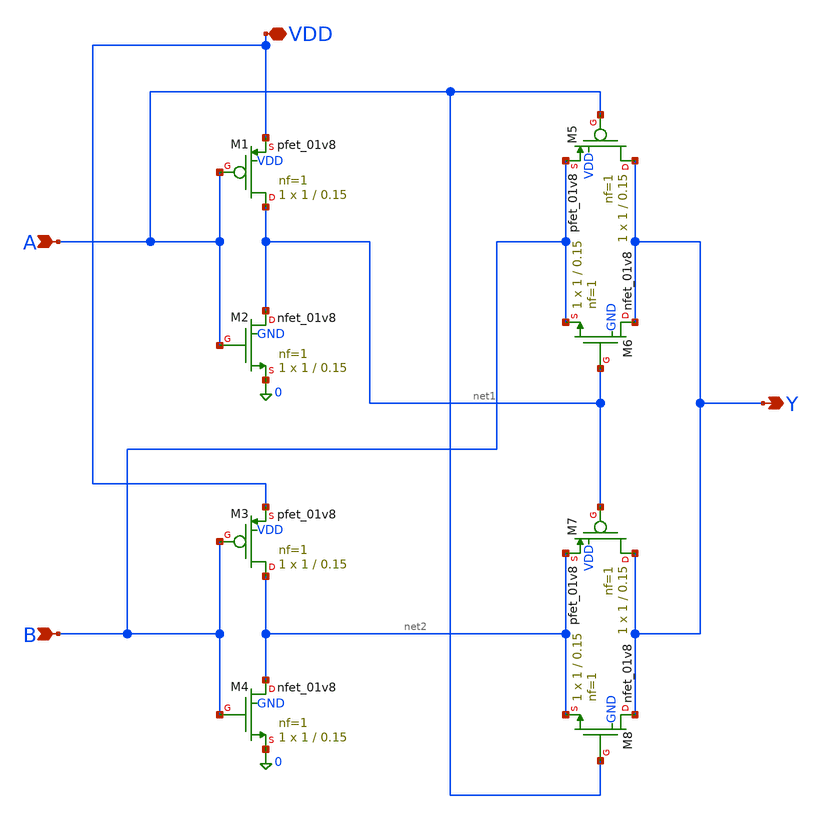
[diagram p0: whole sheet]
** sch_path: schematic/xor.sch
**.subckt xor VDD A B Y
*.iopin VDD
*.ipin A
*.ipin B
*.opin Y
XM1 net1 A VDD VDD sky130_fd_pr__pfet_01v8 L=0.15 W=1 nf=1 ad='int((1 + 1)/2) * 1 / 1 * 0.29' as='int((1 + 2)/2) * 1 / 1 * 0.29'
+ pd='2*int((1 + 1)/2) * (1 / 1 + 0.29)' ps='2*int((1 + 2)/2) * (1 / 1 + 0.29)' nrd='0.29 / 1 ' nrs='0.29 / 1 '
+ sa=0 sb=0 sd=0 mult=1 m=1
XM2 net1 A 0 GND sky130_fd_pr__nfet_01v8 L=0.15 W=1 nf=1 ad='int((1 + 1)/2) * 1 / 1 * 0.29' as='int((1 + 2)/2) * 1 / 1 * 0.29'
+ pd='2*int((1 + 1)/2) * (1 / 1 + 0.29)' ps='2*int((1 + 2)/2) * (1 / 1 + 0.29)' nrd='0.29 / 1 ' nrs='0.29 / 1 '
+ sa=0 sb=0 sd=0 mult=1 m=1
XM3 net2 B VDD VDD sky130_fd_pr__pfet_01v8 L=0.15 W=1 nf=1 ad='int((1 + 1)/2) * 1 / 1 * 0.29' as='int((1 + 2)/2) * 1 / 1 * 0.29'
+ pd='2*int((1 + 1)/2) * (1 / 1 + 0.29)' ps='2*int((1 + 2)/2) * (1 / 1 + 0.29)' nrd='0.29 / 1 ' nrs='0.29 / 1 '
+ sa=0 sb=0 sd=0 mult=1 m=1
XM4 net2 B 0 GND sky130_fd_pr__nfet_01v8 L=0.15 W=1 nf=1 ad='int((1 + 1)/2) * 1 / 1 * 0.29' as='int((1 + 2)/2) * 1 / 1 * 0.29'
+ pd='2*int((1 + 1)/2) * (1 / 1 + 0.29)' ps='2*int((1 + 2)/2) * (1 / 1 + 0.29)' nrd='0.29 / 1 ' nrs='0.29 / 1 '
+ sa=0 sb=0 sd=0 mult=1 m=1
XM5 Y A B VDD sky130_fd_pr__pfet_01v8 L=0.15 W=1 nf=1 ad='int((1 + 1)/2) * 1 / 1 * 0.29' as='int((1 + 2)/2) * 1 / 1 * 0.29'
+ pd='2*int((1 + 1)/2) * (1 / 1 + 0.29)' ps='2*int((1 + 2)/2) * (1 / 1 + 0.29)' nrd='0.29 / 1 ' nrs='0.29 / 1 '
+ sa=0 sb=0 sd=0 mult=1 m=1
XM6 Y net1 B GND sky130_fd_pr__nfet_01v8 L=0.15 W=1 nf=1 ad='int((1 + 1)/2) * 1 / 1 * 0.29' as='int((1 + 2)/2) * 1 / 1 * 0.29'
+ pd='2*int((1 + 1)/2) * (1 / 1 + 0.29)' ps='2*int((1 + 2)/2) * (1 / 1 + 0.29)' nrd='0.29 / 1 ' nrs='0.29 / 1 '
+ sa=0 sb=0 sd=0 mult=1 m=1
XM7 Y net1 net2 VDD sky130_fd_pr__pfet_01v8 L=0.15 W=1 nf=1 ad='int((1 + 1)/2) * 1 / 1 * 0.29' as='int((1 + 2)/2) * 1 / 1 * 0.29'
+ pd='2*int((1 + 1)/2) * (1 / 1 + 0.29)' ps='2*int((1 + 2)/2) * (1 / 1 + 0.29)' nrd='0.29 / 1 ' nrs='0.29 / 1 '
+ sa=0 sb=0 sd=0 mult=1 m=1
XM8 Y A net2 GND sky130_fd_pr__nfet_01v8 L=0.15 W=1 nf=1 ad='int((1 + 1)/2) * 1 / 1 * 0.29' as='int((1 + 2)/2) * 1 / 1 * 0.29'
+ pd='2*int((1 + 1)/2) * (1 / 1 + 0.29)' ps='2*int((1 + 2)/2) * (1 / 1 + 0.29)' nrd='0.29 / 1 ' nrs='0.29 / 1 '
+ sa=0 sb=0 sd=0 mult=1 m=1
**.ends
.end
